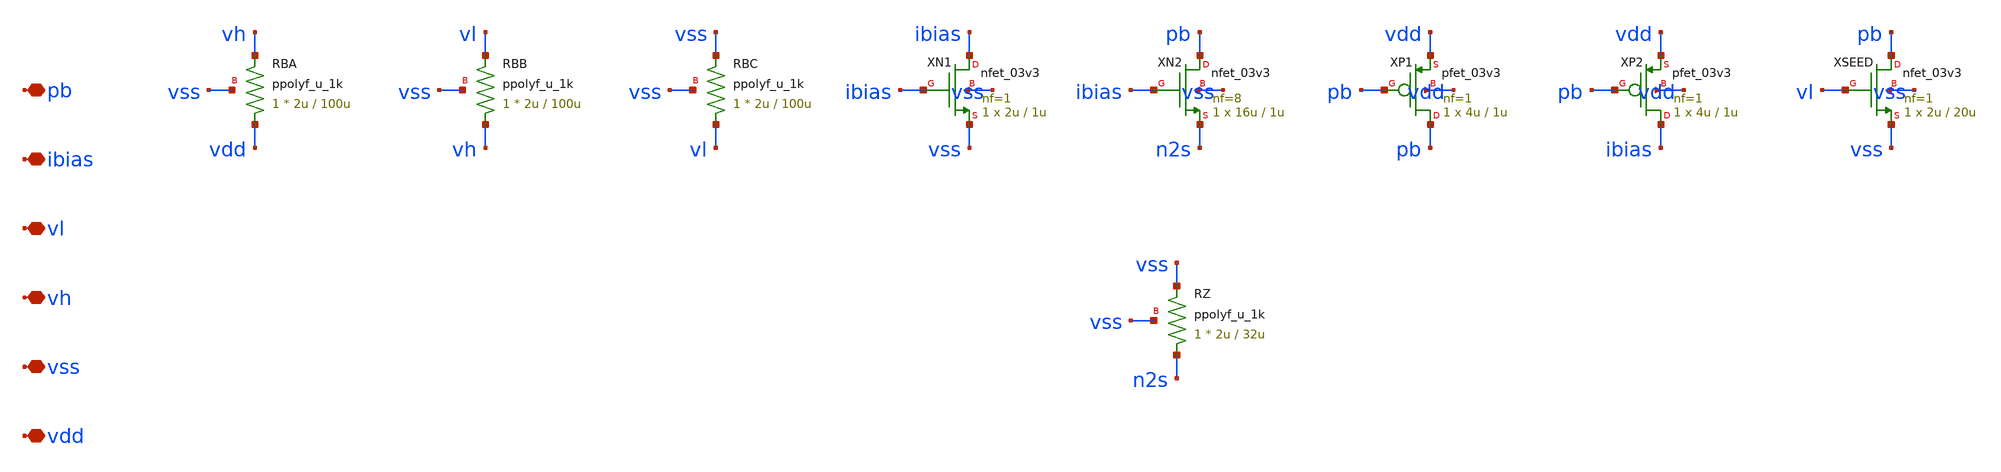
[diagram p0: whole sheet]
** sch_path: design/rcosc_bias.sch
**.subckt rcosc_bias vdd vss vh vl ibias pb
*.iopin vdd
*.iopin vss
*.iopin vh
*.iopin vl
*.iopin ibias
*.iopin pb
XRBA vdd vh vss ppolyf_u_1k r_width=2u r_length=100u m=1
XRBB vh vl vss ppolyf_u_1k r_width=2u r_length=100u m=1
XRBC vl vss vss ppolyf_u_1k r_width=2u r_length=100u m=1
XN1 ibias ibias vss vss nfet_03v3 L=1u W=2u nf=1 ad='int((nf+1)/2) * W/nf * 0.18u' as='int((nf+2)/2) * W/nf * 0.18u'
+ pd='2*int((nf+1)/2) * (W/nf + 0.18u)' ps='2*int((nf+2)/2) * (W/nf + 0.18u)' nrd='0.18u / W' nrs='0.18u / W'
+ sa=0 sb=0 sd=0 m=1
XN2 pb ibias n2s vss nfet_03v3 L=1u W=16u nf=8 ad='int((nf+1)/2) * W/nf * 0.18u' as='int((nf+2)/2) * W/nf * 0.18u'
+ pd='2*int((nf+1)/2) * (W/nf + 0.18u)' ps='2*int((nf+2)/2) * (W/nf + 0.18u)' nrd='0.18u / W' nrs='0.18u / W'
+ sa=0 sb=0 sd=0 m=1
XRZ n2s vss vss ppolyf_u_1k r_width=2u r_length=32u m=1
XP1 pb pb vdd vdd pfet_03v3 L=1u W=4u nf=1 ad='int((nf+1)/2) * W/nf * 0.18u' as='int((nf+2)/2) * W/nf * 0.18u'
+ pd='2*int((nf+1)/2) * (W/nf + 0.18u)' ps='2*int((nf+2)/2) * (W/nf + 0.18u)' nrd='0.18u / W' nrs='0.18u / W'
+ sa=0 sb=0 sd=0 m=1
XP2 ibias pb vdd vdd pfet_03v3 L=1u W=4u nf=1 ad='int((nf+1)/2) * W/nf * 0.18u' as='int((nf+2)/2) * W/nf * 0.18u'
+ pd='2*int((nf+1)/2) * (W/nf + 0.18u)' ps='2*int((nf+2)/2) * (W/nf + 0.18u)' nrd='0.18u / W' nrs='0.18u / W'
+ sa=0 sb=0 sd=0 m=1
XSEED pb vl vss vss nfet_03v3 L=20u W=2u nf=1 ad='int((nf+1)/2) * W/nf * 0.18u' as='int((nf+2)/2) * W/nf * 0.18u'
+ pd='2*int((nf+1)/2) * (W/nf + 0.18u)' ps='2*int((nf+2)/2) * (W/nf + 0.18u)' nrd='0.18u / W' nrs='0.18u / W'
+ sa=0 sb=0 sd=0 m=1
**.ends
.end
